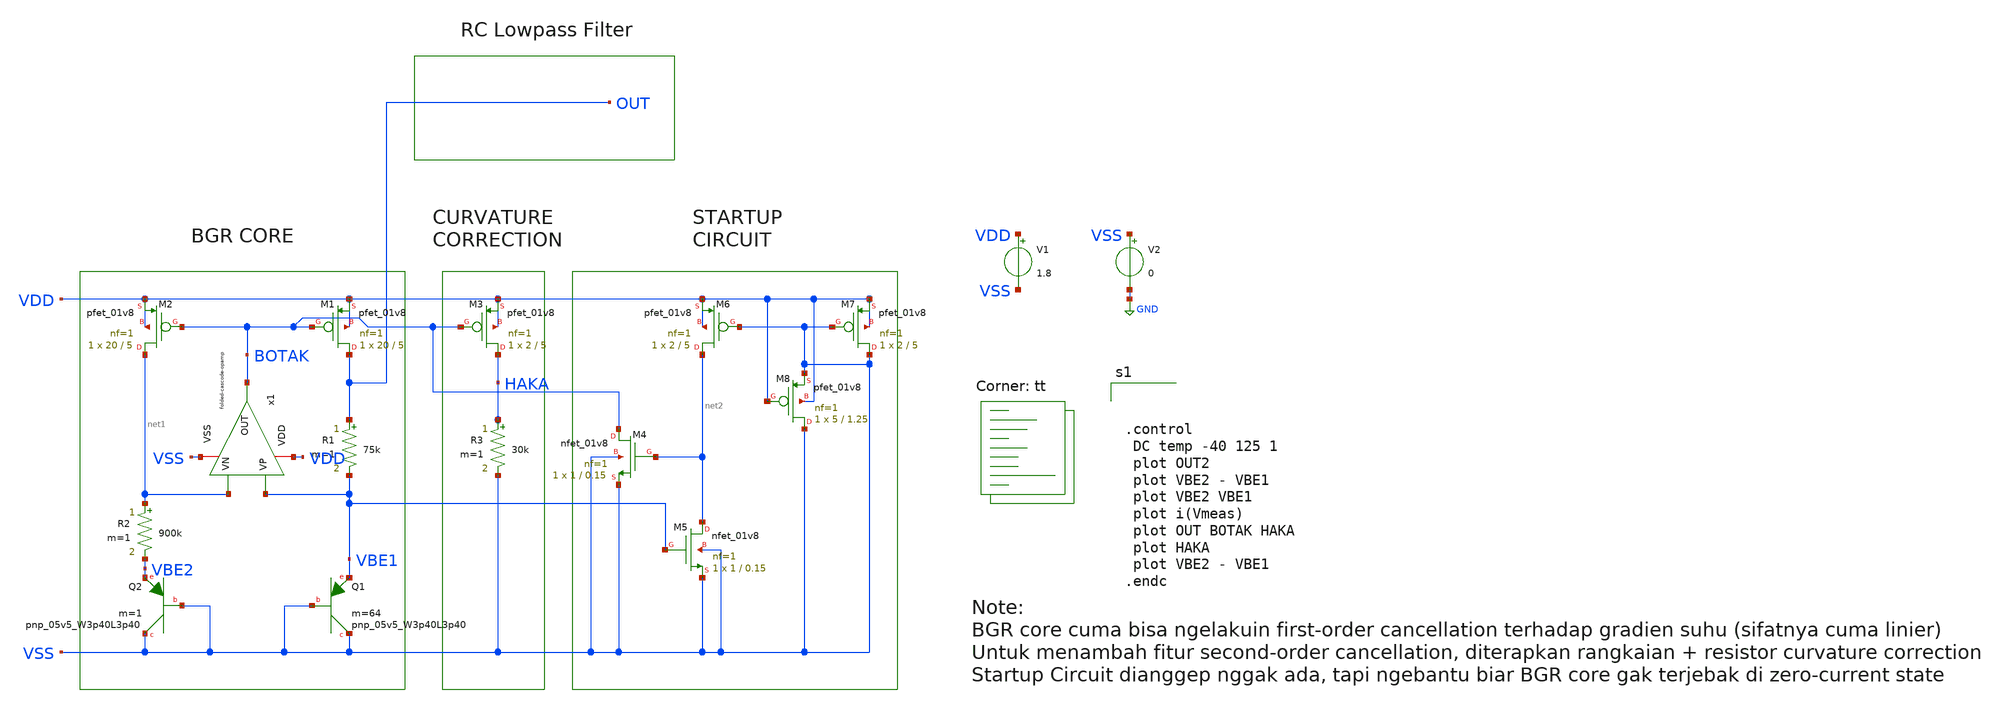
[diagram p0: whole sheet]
** sch_path: bandgap/bgr/bgr-core.sch
**.subckt bgr-core
XM1 OUT BOTAK VDD VDD sky130_fd_pr__pfet_01v8 L=5 W=20 nf=1 ad='int((nf+1)/2) * W/nf * 0.29' as='int((nf+2)/2) * W/nf * 0.29'
+ pd='2*int((nf+1)/2) * (W/nf + 0.29)' ps='2*int((nf+2)/2) * (W/nf + 0.29)' nrd='0.29 / W' nrs='0.29 / W'
+ sa=0 sb=0 sd=0 mult=1 m=1
XM2 net1 BOTAK VDD VDD sky130_fd_pr__pfet_01v8 L=5 W=20 nf=1 ad='int((nf+1)/2) * W/nf * 0.29' as='int((nf+2)/2) * W/nf * 0.29'
+ pd='2*int((nf+1)/2) * (W/nf + 0.29)' ps='2*int((nf+2)/2) * (W/nf + 0.29)' nrd='0.29 / W' nrs='0.29 / W'
+ sa=0 sb=0 sd=0 mult=1 m=1
R1 OUT VBE1 75k m=1
R2 net1 VBE2 900k m=1
XQ1 VSS VSS VBE1 sky130_fd_pr__pnp_05v5_W3p40L3p40 m=64
XQ2 VSS VSS VBE2 sky130_fd_pr__pnp_05v5_W3p40L3p40 m=1
V1 VDD VSS 1.8
V2 VSS GND 0
XM3 HAKA BOTAK VDD VDD sky130_fd_pr__pfet_01v8 L=5 W=2 nf=1 ad='int((nf+1)/2) * W/nf * 0.29' as='int((nf+2)/2) * W/nf * 0.29'
+ pd='2*int((nf+1)/2) * (W/nf + 0.29)' ps='2*int((nf+2)/2) * (W/nf + 0.29)' nrd='0.29 / W' nrs='0.29 / W'
+ sa=0 sb=0 sd=0 mult=1 m=1
R3 HAKA VSS 30k m=1
XM4 BOTAK net2 VSS VSS sky130_fd_pr__nfet_01v8 L=0.15 W=1 nf=1 ad='int((nf+1)/2) * W/nf * 0.29' as='int((nf+2)/2) * W/nf * 0.29'
+ pd='2*int((nf+1)/2) * (W/nf + 0.29)' ps='2*int((nf+2)/2) * (W/nf + 0.29)' nrd='0.29 / W' nrs='0.29 / W'
+ sa=0 sb=0 sd=0 mult=1 m=1
XM5 net2 VBE1 VSS VSS sky130_fd_pr__nfet_01v8 L=0.15 W=1 nf=1 ad='int((nf+1)/2) * W/nf * 0.29' as='int((nf+2)/2) * W/nf * 0.29'
+ pd='2*int((nf+1)/2) * (W/nf + 0.29)' ps='2*int((nf+2)/2) * (W/nf + 0.29)' nrd='0.29 / W' nrs='0.29 / W'
+ sa=0 sb=0 sd=0 mult=1 m=1
XM6 net2 VSS VDD VDD sky130_fd_pr__pfet_01v8 L=5 W=2 nf=1 ad='int((nf+1)/2) * W/nf * 0.29' as='int((nf+2)/2) * W/nf * 0.29'
+ pd='2*int((nf+1)/2) * (W/nf + 0.29)' ps='2*int((nf+2)/2) * (W/nf + 0.29)' nrd='0.29 / W' nrs='0.29 / W'
+ sa=0 sb=0 sd=0 mult=1 m=1
XM7 VSS VSS VDD VDD sky130_fd_pr__pfet_01v8 L=5 W=2 nf=1 ad='int((nf+1)/2) * W/nf * 0.29' as='int((nf+2)/2) * W/nf * 0.29'
+ pd='2*int((nf+1)/2) * (W/nf + 0.29)' ps='2*int((nf+2)/2) * (W/nf + 0.29)' nrd='0.29 / W' nrs='0.29 / W'
+ sa=0 sb=0 sd=0 mult=1 m=1
XM8 VSS VDD VSS VDD sky130_fd_pr__pfet_01v8 L=1.25 W=5 nf=1 ad='int((nf+1)/2) * W/nf * 0.29' as='int((nf+2)/2) * W/nf * 0.29'
+ pd='2*int((nf+1)/2) * (W/nf + 0.29)' ps='2*int((nf+2)/2) * (W/nf + 0.29)' nrd='0.29 / W' nrs='0.29 / W'
+ sa=0 sb=0 sd=0 mult=1 m=1
x1 BOTAK VDD VBE1 net1 VSS folded-cascode-opamp
**** begin user architecture code
.lib $::SKYWATER_MODELS/sky130.lib.spice tt



.control
 DC temp -40 125 1
 plot OUT2
 plot VBE2 - VBE1
 plot VBE2 VBE1
 plot i(Vmeas)
 plot OUT BOTAK HAKA
 plot HAKA
 plot VBE2 - VBE1
.endc


**** end user architecture code
**.ends

* expanding   symbol:  afe-icdec-teknofest-2026/bandgap/bgr-opamp2/folded-cascode-opamp.sym # of
*+ pins=5
** sym_path: bandgap/bgr-opamp2/folded-cascode-opamp.sym
** sch_path: bandgap/bgr-opamp2/folded-cascode-opamp.sch
.subckt folded-cascode-opamp OUT VDD VP VN VSS
*.iopin VSS
*.iopin VDD
*.ipin VP
*.ipin VN
*.opin OUT
XR10 VSS net8 VSS sky130_fd_pr__res_high_po_1p41 L=1.235 mult=1 m=1
XM19 net2 net2 VSS GND sky130_fd_pr__nfet_01v8_lvt L=0.5 W=6.4 nf=1 ad='int((nf+1)/2) * W/nf * 0.29'
+ as='int((nf+2)/2) * W/nf * 0.29' pd='2*int((nf+1)/2) * (W/nf + 0.29)' ps='2*int((nf+2)/2) * (W/nf + 0.29)'
+ nrd='0.29 / W' nrs='0.29 / W' sa=0 sb=0 sd=0 mult=1 m=1
XM20 net3 net2 net9 GND sky130_fd_pr__nfet_01v8_lvt L=0.5 W=6.4 nf=1 ad='int((nf+1)/2) * W/nf * 0.29'
+ as='int((nf+2)/2) * W/nf * 0.29' pd='2*int((nf+1)/2) * (W/nf + 0.29)' ps='2*int((nf+2)/2) * (W/nf + 0.29)'
+ nrd='0.29 / W' nrs='0.29 / W' sa=0 sb=0 sd=0 mult=1 m=1
XM16 net4 net1 VDD VDD sky130_fd_pr__pfet_01v8_lvt L=0.5 W=20.8 nf=1 ad='int((nf+1)/2) * W/nf * 0.29'
+ as='int((nf+2)/2) * W/nf * 0.29' pd='2*int((nf+1)/2) * (W/nf + 0.29)' ps='2*int((nf+2)/2) * (W/nf + 0.29)'
+ nrd='0.29 / W' nrs='0.29 / W' sa=0 sb=0 sd=0 mult=1 m=1
XM13 net1 net1 VDD VDD sky130_fd_pr__pfet_01v8_lvt L=0.5 W=20.8 nf=1 ad='int((nf+1)/2) * W/nf * 0.29'
+ as='int((nf+2)/2) * W/nf * 0.29' pd='2*int((nf+1)/2) * (W/nf + 0.29)' ps='2*int((nf+2)/2) * (W/nf + 0.29)'
+ nrd='0.29 / W' nrs='0.29 / W' sa=0 sb=0 sd=0 mult=1 m=1
XM14 net2 net3 net4 VDD sky130_fd_pr__pfet_01v8_lvt L=0.5 W=20.8 nf=1 ad='int((nf+1)/2) * W/nf * 0.29'
+ as='int((nf+2)/2) * W/nf * 0.29' pd='2*int((nf+1)/2) * (W/nf + 0.29)' ps='2*int((nf+2)/2) * (W/nf + 0.29)'
+ nrd='0.29 / W' nrs='0.29 / W' sa=0 sb=0 sd=0 mult=1 m=1
XM17 net3 net3 net1 VDD sky130_fd_pr__pfet_01v8_lvt L=0.5 W=20.8 nf=1 ad='int((nf+1)/2) * W/nf * 0.29'
+ as='int((nf+2)/2) * W/nf * 0.29' pd='2*int((nf+1)/2) * (W/nf + 0.29)' ps='2*int((nf+2)/2) * (W/nf + 0.29)'
+ nrd='0.29 / W' nrs='0.29 / W' sa=0 sb=0 sd=0 mult=1 m=1
XM18 net10 net1 VDD VDD sky130_fd_pr__pfet_01v8_lvt L=0.5 W=20.8 nf=1 ad='int((nf+1)/2) * W/nf * 0.29'
+ as='int((nf+2)/2) * W/nf * 0.29' pd='2*int((nf+1)/2) * (W/nf + 0.29)' ps='2*int((nf+2)/2) * (W/nf + 0.29)'
+ nrd='0.29 / W' nrs='0.29 / W' sa=0 sb=0 sd=0 mult=1 m=1
XM21 net11 net3 net10 VDD sky130_fd_pr__pfet_01v8_lvt L=0.5 W=20.8 nf=1 ad='int((nf+1)/2) * W/nf * 0.29'
+ as='int((nf+2)/2) * W/nf * 0.29' pd='2*int((nf+1)/2) * (W/nf + 0.29)' ps='2*int((nf+2)/2) * (W/nf + 0.29)'
+ nrd='0.29 / W' nrs='0.29 / W' sa=0 sb=0 sd=0 mult=1 m=1
XM22 net11 net11 net13 GND sky130_fd_pr__nfet_01v8_lvt L=0.5 W=1.45 nf=1 ad='int((nf+1)/2) * W/nf * 0.29'
+ as='int((nf+2)/2) * W/nf * 0.29' pd='2*int((nf+1)/2) * (W/nf + 0.29)' ps='2*int((nf+2)/2) * (W/nf + 0.29)'
+ nrd='0.29 / W' nrs='0.29 / W' sa=0 sb=0 sd=0 mult=1 m=1
XM23 net13 net11 net12 GND sky130_fd_pr__nfet_01v8_lvt L=0.5 W=1.45 nf=1 ad='int((nf+1)/2) * W/nf * 0.29'
+ as='int((nf+2)/2) * W/nf * 0.29' pd='2*int((nf+1)/2) * (W/nf + 0.29)' ps='2*int((nf+2)/2) * (W/nf + 0.29)'
+ nrd='0.29 / W' nrs='0.29 / W' sa=0 sb=0 sd=0 mult=1 m=1
XM24 net12 net11 VSS GND sky130_fd_pr__nfet_01v8_lvt L=0.5 W=1.45 nf=1 ad='int((nf+1)/2) * W/nf * 0.29'
+ as='int((nf+2)/2) * W/nf * 0.29' pd='2*int((nf+1)/2) * (W/nf + 0.29)' ps='2*int((nf+2)/2) * (W/nf + 0.29)'
+ nrd='0.29 / W' nrs='0.29 / W' sa=0 sb=0 sd=0 mult=1 m=1
XM26 net19 VN net14 VDD sky130_fd_pr__pfet_01v8_lvt L=1.25 W=64 nf=1 ad='int((nf+1)/2) * W/nf * 0.29'
+ as='int((nf+2)/2) * W/nf * 0.29' pd='2*int((nf+1)/2) * (W/nf + 0.29)' ps='2*int((nf+2)/2) * (W/nf + 0.29)'
+ nrd='0.29 / W' nrs='0.29 / W' sa=0 sb=0 sd=0 mult=1 m=1
XM27 net18 VP net14 VDD sky130_fd_pr__pfet_01v8_lvt L=1.25 W=64 nf=1 ad='int((nf+1)/2) * W/nf * 0.29'
+ as='int((nf+2)/2) * W/nf * 0.29' pd='2*int((nf+1)/2) * (W/nf + 0.29)' ps='2*int((nf+2)/2) * (W/nf + 0.29)'
+ nrd='0.29 / W' nrs='0.29 / W' sa=0 sb=0 sd=0 mult=1 m=1
XM15 net14 net20 VDD VDD sky130_fd_pr__pfet_01v8_lvt L=1.25 W=10.8 nf=1 ad='int((nf+1)/2) * W/nf * 0.29'
+ as='int((nf+2)/2) * W/nf * 0.29' pd='2*int((nf+1)/2) * (W/nf + 0.29)' ps='2*int((nf+2)/2) * (W/nf + 0.29)'
+ nrd='0.29 / W' nrs='0.29 / W' sa=0 sb=0 sd=0 mult=1 m=1
XM25 net16 net1 VDD VDD sky130_fd_pr__pfet_01v8_lvt L=1.25 W=10.4 nf=1 ad='int((nf+1)/2) * W/nf * 0.29'
+ as='int((nf+2)/2) * W/nf * 0.29' pd='2*int((nf+1)/2) * (W/nf + 0.29)' ps='2*int((nf+2)/2) * (W/nf + 0.29)'
+ nrd='0.29 / W' nrs='0.29 / W' sa=0 sb=0 sd=0 mult=1 m=1
XM28 net17 net1 VDD VDD sky130_fd_pr__pfet_01v8_lvt L=1.25 W=10.4 nf=1 ad='int((nf+1)/2) * W/nf * 0.29'
+ as='int((nf+2)/2) * W/nf * 0.29' pd='2*int((nf+1)/2) * (W/nf + 0.29)' ps='2*int((nf+2)/2) * (W/nf + 0.29)'
+ nrd='0.29 / W' nrs='0.29 / W' sa=0 sb=0 sd=0 mult=1 m=1
XM29 OUT net3 net16 VDD sky130_fd_pr__pfet_01v8_lvt L=1.25 W=10.4 nf=1 ad='int((nf+1)/2) * W/nf * 0.29'
+ as='int((nf+2)/2) * W/nf * 0.29' pd='2*int((nf+1)/2) * (W/nf + 0.29)' ps='2*int((nf+2)/2) * (W/nf + 0.29)'
+ nrd='0.29 / W' nrs='0.29 / W' sa=0 sb=0 sd=0 mult=1 m=1
XM30 net15 net3 net17 VDD sky130_fd_pr__pfet_01v8_lvt L=1.25 W=10.4 nf=1 ad='int((nf+1)/2) * W/nf * 0.29'
+ as='int((nf+2)/2) * W/nf * 0.29' pd='2*int((nf+1)/2) * (W/nf + 0.29)' ps='2*int((nf+2)/2) * (W/nf + 0.29)'
+ nrd='0.29 / W' nrs='0.29 / W' sa=0 sb=0 sd=0 mult=1 m=1
XM31 OUT net11 net19 GND sky130_fd_pr__nfet_01v8_lvt L=1.25 W=3.4 nf=1 ad='int((nf+1)/2) * W/nf * 0.29'
+ as='int((nf+2)/2) * W/nf * 0.29' pd='2*int((nf+1)/2) * (W/nf + 0.29)' ps='2*int((nf+2)/2) * (W/nf + 0.29)'
+ nrd='0.29 / W' nrs='0.29 / W' sa=0 sb=0 sd=0 mult=1 m=1
XM32 net15 net11 net18 GND sky130_fd_pr__nfet_01v8_lvt L=1.25 W=3.4 nf=1 ad='int((nf+1)/2) * W/nf * 0.29'
+ as='int((nf+2)/2) * W/nf * 0.29' pd='2*int((nf+1)/2) * (W/nf + 0.29)' ps='2*int((nf+2)/2) * (W/nf + 0.29)'
+ nrd='0.29 / W' nrs='0.29 / W' sa=0 sb=0 sd=0 mult=1 m=1
XM33 net19 net15 VSS GND sky130_fd_pr__nfet_01v8_lvt L=1.25 W=3.4 nf=1 ad='int((nf+1)/2) * W/nf * 0.29'
+ as='int((nf+2)/2) * W/nf * 0.29' pd='2*int((nf+1)/2) * (W/nf + 0.29)' ps='2*int((nf+2)/2) * (W/nf + 0.29)'
+ nrd='0.29 / W' nrs='0.29 / W' sa=0 sb=0 sd=0 mult=1 m=1
XM34 net18 net15 VSS GND sky130_fd_pr__nfet_01v8_lvt L=1.25 W=3.4 nf=1 ad='int((nf+1)/2) * W/nf * 0.29'
+ as='int((nf+2)/2) * W/nf * 0.29' pd='2*int((nf+1)/2) * (W/nf + 0.29)' ps='2*int((nf+2)/2) * (W/nf + 0.29)'
+ nrd='0.29 / W' nrs='0.29 / W' sa=0 sb=0 sd=0 mult=1 m=1
XM35 net20 net20 VDD VDD sky130_fd_pr__pfet_01v8_lvt L=1.25 W=10.8 nf=1 ad='int((nf+1)/2) * W/nf * 0.29'
+ as='int((nf+2)/2) * W/nf * 0.29' pd='2*int((nf+1)/2) * (W/nf + 0.29)' ps='2*int((nf+2)/2) * (W/nf + 0.29)'
+ nrd='0.29 / W' nrs='0.29 / W' sa=0 sb=0 sd=0 mult=1 m=1
XR6 VSS net23 VSS sky130_fd_pr__res_high_po_1p41 L=500 mult=1 m=1
XR1 net23 net21 VSS sky130_fd_pr__res_high_po_1p41 L=500 mult=1 m=1
XR2 net21 net22 VSS sky130_fd_pr__res_high_po_1p41 L=500 mult=1 m=1
XR3 net22 net24 VSS sky130_fd_pr__res_high_po_1p41 L=500 mult=1 m=1
XR4 net24 net20 VSS sky130_fd_pr__res_high_po_1p41 L=500 mult=1 m=1
XR5 net8 net6 VSS sky130_fd_pr__res_high_po_1p41 L=1.235 mult=1 m=1
XR7 net6 net7 VSS sky130_fd_pr__res_high_po_1p41 L=1.235 mult=1 m=1
XR8 net7 net5 VSS sky130_fd_pr__res_high_po_1p41 L=1.235 mult=1 m=1
XR9 net5 net9 VSS sky130_fd_pr__res_high_po_1p41 L=1.235 mult=1 m=1
.ends

.GLOBAL GND
.end
